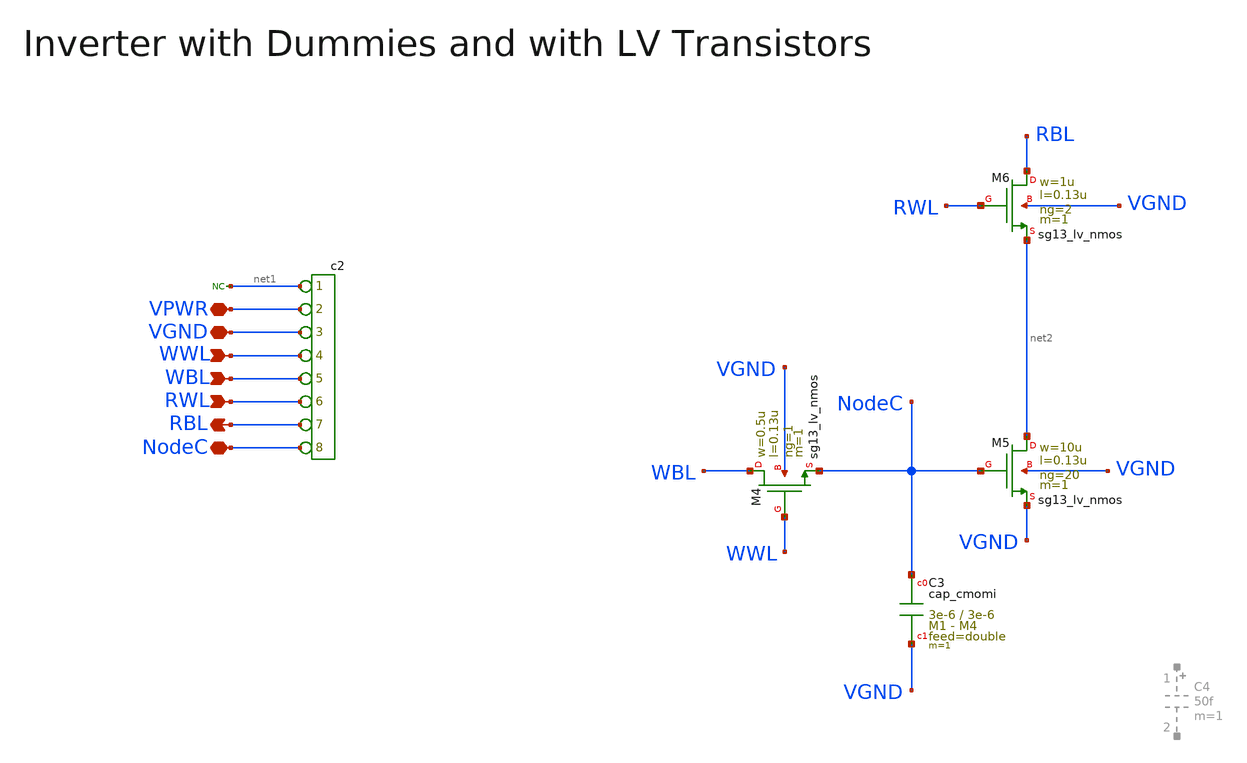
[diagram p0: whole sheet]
** sch_path: macros/heichips26_analog_project/macros/dramcell_2_0/schematic/xschem/dramcell_2_0.sch
**.subckt dramcell_2_0 RBL WWL WBL RWL VPWR VGND NodeC
*.opin RBL
*.ipin WWL
*.ipin WBL
*.ipin RWL
*.iopin VPWR
*.iopin VGND
*.iopin NodeC
*connector(8,1) ?1 net1 ?1 VPWR ?1 VGND ?1 WWL ?1 WBL ?1 RWL ?1 RBL ?1 NodeC
* noconn #net1
XM4 WBL WWL NodeC VGND sg13_lv_nmos w=0.5u l=0.13u ng=1 m=1 mm_ok=1
XC3 NodeC VGND cap_cmomi w=3e-6 l=3e-6 mmin=1 mmax=4 feed=double subblock=0 m=1 mm_ok=1
XM5 net2 NodeC VGND VGND sg13_lv_nmos w=10u l=0.13u ng=20 m=1 mm_ok=1
XM6 RBL RWL net2 VGND sg13_lv_nmos w=1u l=0.13u ng=2 m=1 mm_ok=1
**.ends
.end
